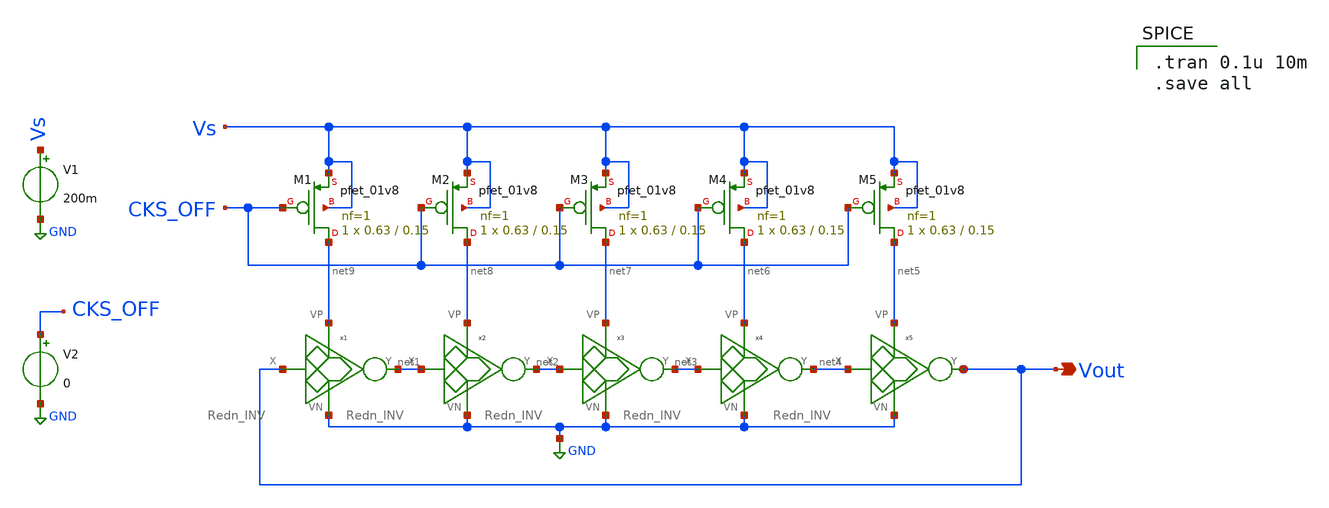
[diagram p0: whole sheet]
** sch_path: Blocks/Rng_Osc_with_Contrl_logic/Rng_Osc_wth_Cntrl_lgc.sch
**.subckt Rng_Osc_wth_Cntrl_lgc Vout
*.opin Vout
V1 Vs GND 200m
XM1 net9 CKS_OFF Vs Vs sky130_fd_pr__pfet_01v8 L=0.15 W=0.63 nf=1 ad='int((nf+1)/2) * W/nf * 0.29' as='int((nf+2)/2) * W/nf * 0.29'
+ pd='2*int((nf+1)/2) * (W/nf + 0.29)' ps='2*int((nf+2)/2) * (W/nf + 0.29)' nrd='0.29 / W' nrs='0.29 / W'
+ sa=0 sb=0 sd=0 mult=1 m=1
XM2 net8 CKS_OFF Vs Vs sky130_fd_pr__pfet_01v8 L=0.15 W=0.63 nf=1 ad='int((nf+1)/2) * W/nf * 0.29' as='int((nf+2)/2) * W/nf * 0.29'
+ pd='2*int((nf+1)/2) * (W/nf + 0.29)' ps='2*int((nf+2)/2) * (W/nf + 0.29)' nrd='0.29 / W' nrs='0.29 / W'
+ sa=0 sb=0 sd=0 mult=1 m=1
XM3 net7 CKS_OFF Vs Vs sky130_fd_pr__pfet_01v8 L=0.15 W=0.63 nf=1 ad='int((nf+1)/2) * W/nf * 0.29' as='int((nf+2)/2) * W/nf * 0.29'
+ pd='2*int((nf+1)/2) * (W/nf + 0.29)' ps='2*int((nf+2)/2) * (W/nf + 0.29)' nrd='0.29 / W' nrs='0.29 / W'
+ sa=0 sb=0 sd=0 mult=1 m=1
XM4 net6 CKS_OFF Vs Vs sky130_fd_pr__pfet_01v8 L=0.15 W=0.63 nf=1 ad='int((nf+1)/2) * W/nf * 0.29' as='int((nf+2)/2) * W/nf * 0.29'
+ pd='2*int((nf+1)/2) * (W/nf + 0.29)' ps='2*int((nf+2)/2) * (W/nf + 0.29)' nrd='0.29 / W' nrs='0.29 / W'
+ sa=0 sb=0 sd=0 mult=1 m=1
XM5 net5 CKS_OFF Vs Vs sky130_fd_pr__pfet_01v8 L=0.15 W=0.63 nf=1 ad='int((nf+1)/2) * W/nf * 0.29' as='int((nf+2)/2) * W/nf * 0.29'
+ pd='2*int((nf+1)/2) * (W/nf + 0.29)' ps='2*int((nf+2)/2) * (W/nf + 0.29)' nrd='0.29 / W' nrs='0.29 / W'
+ sa=0 sb=0 sd=0 mult=1 m=1
V2 CKS_OFF GND 0
x1 Vout net1 net9 GND Redn_INV
x2 net1 net2 net8 GND Redn_INV
x3 net2 net3 net7 GND Redn_INV
x4 net3 net4 net6 GND Redn_INV
x5 net4 Vout net5 GND Redn_INV
**** begin user architecture code

** opencircuitdesign pdks install
.lib $::SKYWATER_MODELS/sky130.lib.spice tt



.tran 0.1u 10m
.save all

**** end user architecture code
**.ends

* expanding   symbol:  component/Reduntant_Inverter/Redn_INV.sym # of pins=4
** sym_path: component/Reduntant_Inverter/Redn_INV.sym
** sch_path: component/Reduntant_Inverter/Redn_INV.sch
.subckt Redn_INV X Y VP VN
*.opin Y
*.ipin X
*.iopin VP
*.iopin VN
XM15 net4 X VN VN sky130_fd_pr__nfet_01v8_lvt L=0.15 W=1 nf=1 ad='int((nf+1)/2) * W/nf * 0.29' as='int((nf+2)/2) * W/nf * 0.29'
+ pd='2*int((nf+1)/2) * (W/nf + 0.29)' ps='2*int((nf+2)/2) * (W/nf + 0.29)' nrd='0.29 / W' nrs='0.29 / W'
+ sa=0 sb=0 sd=0 mult=1 m=1
XM1 net5 X net3 VN sky130_fd_pr__nfet_01v8_lvt L=0.15 W=3.25 nf=1 ad='int((nf+1)/2) * W/nf * 0.29' as='int((nf+2)/2) * W/nf * 0.29'
+ pd='2*int((nf+1)/2) * (W/nf + 0.29)' ps='2*int((nf+2)/2) * (W/nf + 0.29)' nrd='0.29 / W' nrs='0.29 / W'
+ sa=0 sb=0 sd=0 mult=1 m=1
XM16 Y X net6 VN sky130_fd_pr__nfet_01v8_lvt L=0.15 W=6.5 nf=1 ad='int((nf+1)/2) * W/nf * 0.29' as='int((nf+2)/2) * W/nf * 0.29'
+ pd='2*int((nf+1)/2) * (W/nf + 0.29)' ps='2*int((nf+2)/2) * (W/nf + 0.29)' nrd='0.29 / W' nrs='0.29 / W'
+ sa=0 sb=0 sd=0 mult=1 m=1
XM17 net3 X VN VN sky130_fd_pr__nfet_01v8_lvt L=0.15 W=3.25 nf=1 ad='int((nf+1)/2) * W/nf * 0.29' as='int((nf+2)/2) * W/nf * 0.29'
+ pd='2*int((nf+1)/2) * (W/nf + 0.29)' ps='2*int((nf+2)/2) * (W/nf + 0.29)' nrd='0.29 / W' nrs='0.29 / W'
+ sa=0 sb=0 sd=0 mult=1 m=1
XM18 net2 X VN VN sky130_fd_pr__nfet_01v8_lvt L=0.15 W=1.5 nf=1 ad='int((nf+1)/2) * W/nf * 0.29' as='int((nf+2)/2) * W/nf * 0.29'
+ pd='2*int((nf+1)/2) * (W/nf + 0.29)' ps='2*int((nf+2)/2) * (W/nf + 0.29)' nrd='0.29 / W' nrs='0.29 / W'
+ sa=0 sb=0 sd=0 mult=1 m=1
XM19 net1 X VN VN sky130_fd_pr__nfet_01v8_lvt L=0.15 W=6.5 nf=1 ad='int((nf+1)/2) * W/nf * 0.29' as='int((nf+2)/2) * W/nf * 0.29'
+ pd='2*int((nf+1)/2) * (W/nf + 0.29)' ps='2*int((nf+2)/2) * (W/nf + 0.29)' nrd='0.29 / W' nrs='0.29 / W'
+ sa=0 sb=0 sd=0 mult=1 m=1
XM20 net6 X net1 VN sky130_fd_pr__nfet_01v8_lvt L=0.15 W=6.5 nf=1 ad='int((nf+1)/2) * W/nf * 0.29' as='int((nf+2)/2) * W/nf * 0.29'
+ pd='2*int((nf+1)/2) * (W/nf + 0.29)' ps='2*int((nf+2)/2) * (W/nf + 0.29)' nrd='0.29 / W' nrs='0.29 / W'
+ sa=0 sb=0 sd=0 mult=1 m=1
XM2 net4 X VP VP sky130_fd_pr__pfet_01v8 L=0.15 W=10 nf=1 ad='int((nf+1)/2) * W/nf * 0.29' as='int((nf+2)/2) * W/nf * 0.29'
+ pd='2*int((nf+1)/2) * (W/nf + 0.29)' ps='2*int((nf+2)/2) * (W/nf + 0.29)' nrd='0.29 / W' nrs='0.29 / W'
+ sa=0 sb=0 sd=0 mult=1 m=1
XM5 net5 X net4 net4 sky130_fd_pr__pfet_01v8 L=0.15 W=10 nf=1 ad='int((nf+1)/2) * W/nf * 0.29' as='int((nf+2)/2) * W/nf * 0.29'
+ pd='2*int((nf+1)/2) * (W/nf + 0.29)' ps='2*int((nf+2)/2) * (W/nf + 0.29)' nrd='0.29 / W' nrs='0.29 / W'
+ sa=0 sb=0 sd=0 mult=1 m=1
XM6 Y X net5 VP sky130_fd_pr__pfet_01v8 L=0.15 W=10 nf=1 ad='int((nf+1)/2) * W/nf * 0.29' as='int((nf+2)/2) * W/nf * 0.29'
+ pd='2*int((nf+1)/2) * (W/nf + 0.29)' ps='2*int((nf+2)/2) * (W/nf + 0.29)' nrd='0.29 / W' nrs='0.29 / W'
+ sa=0 sb=0 sd=0 mult=1 m=1
XM8 net3 X VP VP sky130_fd_pr__pfet_01v8 L=0.15 W=2 nf=1 ad='int((nf+1)/2) * W/nf * 0.29' as='int((nf+2)/2) * W/nf * 0.29'
+ pd='2*int((nf+1)/2) * (W/nf + 0.29)' ps='2*int((nf+2)/2) * (W/nf + 0.29)' nrd='0.29 / W' nrs='0.29 / W'
+ sa=0 sb=0 sd=0 mult=1 m=1
XM12 net2 X VP VP sky130_fd_pr__pfet_01v8 L=0.15 W=5 nf=1 ad='int((nf+1)/2) * W/nf * 0.29' as='int((nf+2)/2) * W/nf * 0.29'
+ pd='2*int((nf+1)/2) * (W/nf + 0.29)' ps='2*int((nf+2)/2) * (W/nf + 0.29)' nrd='0.29 / W' nrs='0.29 / W'
+ sa=0 sb=0 sd=0 mult=1 m=1
XM14 net6 X net2 VP sky130_fd_pr__pfet_01v8 L=0.15 W=5 nf=1 ad='int((nf+1)/2) * W/nf * 0.29' as='int((nf+2)/2) * W/nf * 0.29'
+ pd='2*int((nf+1)/2) * (W/nf + 0.29)' ps='2*int((nf+2)/2) * (W/nf + 0.29)' nrd='0.29 / W' nrs='0.29 / W'
+ sa=0 sb=0 sd=0 mult=1 m=1
XM21 net1 X VP VP sky130_fd_pr__pfet_01v8 L=0.15 W=1.5 nf=1 ad='int((nf+1)/2) * W/nf * 0.29' as='int((nf+2)/2) * W/nf * 0.29'
+ pd='2*int((nf+1)/2) * (W/nf + 0.29)' ps='2*int((nf+2)/2) * (W/nf + 0.29)' nrd='0.29 / W' nrs='0.29 / W'
+ sa=0 sb=0 sd=0 mult=1 m=1
.ends

.GLOBAL GND
.end
